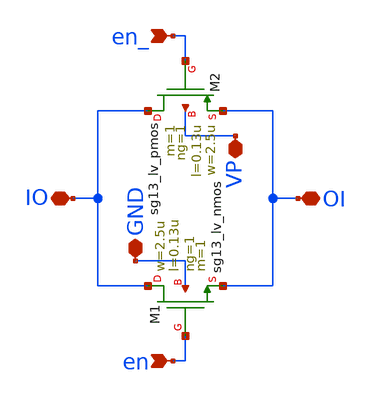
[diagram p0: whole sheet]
** sch_path: PLL0663-main/schematic/xschem/divider/vco_passgate_mux.sch
**.subckt vco_passgate_mux OI IO VP GND en_ en
*.iopin OI
*.iopin IO
*.iopin VP
*.iopin GND
*.ipin en_
*.ipin en
XM1 IO en OI GND sg13_lv_nmos w=2.5u l=0.13u ng=1 m=1 mm_ok=1
XM2 IO en_ OI VP sg13_lv_pmos w=2.5u l=0.13u ng=1 m=1 mm_ok=1
**.ends
.end
